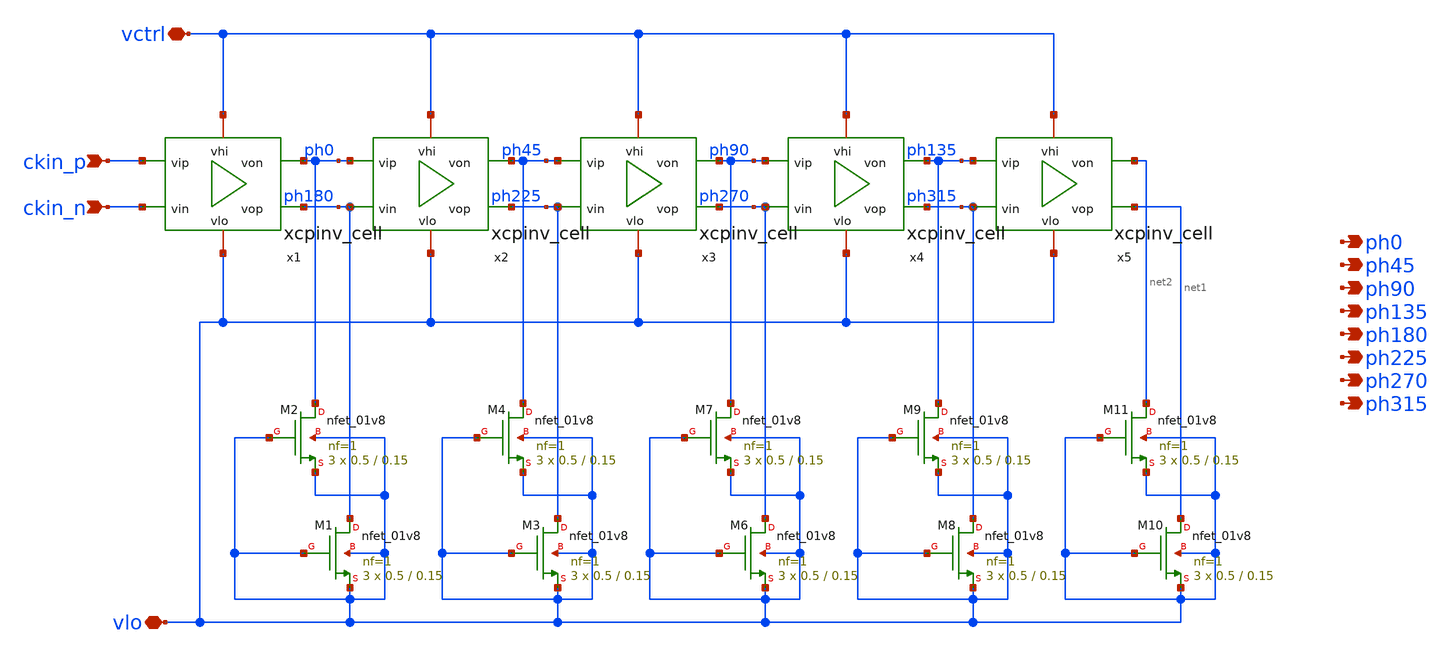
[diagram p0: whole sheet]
** sch_path: xschem/ILMPCG_delayline.sch
**.subckt ILMPCG_delayline vctrl ckin_p ckin_n ph0 ph45 ph90 ph135 ph180 ph225 ph270 ph315 vlo
*.iopin vctrl
*.ipin ckin_p
*.ipin ckin_n
*.opin ph0
*.opin ph45
*.opin ph90
*.opin ph135
*.opin ph180
*.opin ph225
*.opin ph270
*.opin ph315
*.iopin vlo
x1 vctrl ckin_p ckin_n vlo ph180 ph0 xcpinv_cell
x2 vctrl ph0 ph180 vlo ph225 ph45 xcpinv_cell
XM1 ph180 vlo vlo vlo sky130_fd_pr__nfet_01v8 L=0.15 W=0.5 nf=1 ad='int((nf+1)/2) * W/nf * 0.29' as='int((nf+2)/2) * W/nf * 0.29'
+ pd='2*int((nf+1)/2) * (W/nf + 0.29)' ps='2*int((nf+2)/2) * (W/nf + 0.29)' nrd='0.29 / W' nrs='0.29 / W'
+ sa=0 sb=0 sd=0 mult=3 m=3
XM2 ph0 vlo vlo vlo sky130_fd_pr__nfet_01v8 L=0.15 W=0.5 nf=1 ad='int((nf+1)/2) * W/nf * 0.29' as='int((nf+2)/2) * W/nf * 0.29'
+ pd='2*int((nf+1)/2) * (W/nf + 0.29)' ps='2*int((nf+2)/2) * (W/nf + 0.29)' nrd='0.29 / W' nrs='0.29 / W'
+ sa=0 sb=0 sd=0 mult=3 m=3
XM3 ph225 vlo vlo vlo sky130_fd_pr__nfet_01v8 L=0.15 W=0.5 nf=1 ad='int((nf+1)/2) * W/nf * 0.29' as='int((nf+2)/2) * W/nf * 0.29'
+ pd='2*int((nf+1)/2) * (W/nf + 0.29)' ps='2*int((nf+2)/2) * (W/nf + 0.29)' nrd='0.29 / W' nrs='0.29 / W'
+ sa=0 sb=0 sd=0 mult=3 m=3
XM4 ph45 vlo vlo vlo sky130_fd_pr__nfet_01v8 L=0.15 W=0.5 nf=1 ad='int((nf+1)/2) * W/nf * 0.29' as='int((nf+2)/2) * W/nf * 0.29'
+ pd='2*int((nf+1)/2) * (W/nf + 0.29)' ps='2*int((nf+2)/2) * (W/nf + 0.29)' nrd='0.29 / W' nrs='0.29 / W'
+ sa=0 sb=0 sd=0 mult=3 m=3
x3 vctrl ph45 ph225 vlo ph270 ph90 xcpinv_cell
XM6 ph270 vlo vlo vlo sky130_fd_pr__nfet_01v8 L=0.15 W=0.5 nf=1 ad='int((nf+1)/2) * W/nf * 0.29' as='int((nf+2)/2) * W/nf * 0.29'
+ pd='2*int((nf+1)/2) * (W/nf + 0.29)' ps='2*int((nf+2)/2) * (W/nf + 0.29)' nrd='0.29 / W' nrs='0.29 / W'
+ sa=0 sb=0 sd=0 mult=3 m=3
XM7 ph90 vlo vlo vlo sky130_fd_pr__nfet_01v8 L=0.15 W=0.5 nf=1 ad='int((nf+1)/2) * W/nf * 0.29' as='int((nf+2)/2) * W/nf * 0.29'
+ pd='2*int((nf+1)/2) * (W/nf + 0.29)' ps='2*int((nf+2)/2) * (W/nf + 0.29)' nrd='0.29 / W' nrs='0.29 / W'
+ sa=0 sb=0 sd=0 mult=3 m=3
x4 vctrl ph90 ph270 vlo ph315 ph135 xcpinv_cell
XM8 ph315 vlo vlo vlo sky130_fd_pr__nfet_01v8 L=0.15 W=0.5 nf=1 ad='int((nf+1)/2) * W/nf * 0.29' as='int((nf+2)/2) * W/nf * 0.29'
+ pd='2*int((nf+1)/2) * (W/nf + 0.29)' ps='2*int((nf+2)/2) * (W/nf + 0.29)' nrd='0.29 / W' nrs='0.29 / W'
+ sa=0 sb=0 sd=0 mult=3 m=3
XM9 ph135 vlo vlo vlo sky130_fd_pr__nfet_01v8 L=0.15 W=0.5 nf=1 ad='int((nf+1)/2) * W/nf * 0.29' as='int((nf+2)/2) * W/nf * 0.29'
+ pd='2*int((nf+1)/2) * (W/nf + 0.29)' ps='2*int((nf+2)/2) * (W/nf + 0.29)' nrd='0.29 / W' nrs='0.29 / W'
+ sa=0 sb=0 sd=0 mult=3 m=3
x5 vctrl ph135 ph315 vlo net1 net2 xcpinv_cell
XM10 net1 vlo vlo vlo sky130_fd_pr__nfet_01v8 L=0.15 W=0.5 nf=1 ad='int((nf+1)/2) * W/nf * 0.29' as='int((nf+2)/2) * W/nf * 0.29'
+ pd='2*int((nf+1)/2) * (W/nf + 0.29)' ps='2*int((nf+2)/2) * (W/nf + 0.29)' nrd='0.29 / W' nrs='0.29 / W'
+ sa=0 sb=0 sd=0 mult=3 m=3
XM11 net2 vlo vlo vlo sky130_fd_pr__nfet_01v8 L=0.15 W=0.5 nf=1 ad='int((nf+1)/2) * W/nf * 0.29' as='int((nf+2)/2) * W/nf * 0.29'
+ pd='2*int((nf+1)/2) * (W/nf + 0.29)' ps='2*int((nf+2)/2) * (W/nf + 0.29)' nrd='0.29 / W' nrs='0.29 / W'
+ sa=0 sb=0 sd=0 mult=3 m=3
**.ends

* expanding   symbol:  xcpinv_cell.sym # of pins=6
** sym_path: xschem/xcpinv_cell.sym
** sch_path: xschem/xcpinv_cell.sch
.subckt xcpinv_cell vhi vip vin vlo vop von
*.iopin vhi
*.iopin vlo
*.ipin vip
*.ipin vin
*.opin von
*.opin vop
XM1 von vip vhi vhi sky130_fd_pr__pfet_01v8 L=0.15 W=16 nf=1 ad='int((nf+1)/2) * W/nf * 0.29' as='int((nf+2)/2) * W/nf * 0.29'
+ pd='2*int((nf+1)/2) * (W/nf + 0.29)' ps='2*int((nf+2)/2) * (W/nf + 0.29)' nrd='0.29 / W' nrs='0.29 / W'
+ sa=0 sb=0 sd=0 mult=1 m=1
XM2 von vip vlo vlo sky130_fd_pr__nfet_01v8 L=0.15 W=8 nf=1 ad='int((nf+1)/2) * W/nf * 0.29' as='int((nf+2)/2) * W/nf * 0.29'
+ pd='2*int((nf+1)/2) * (W/nf + 0.29)' ps='2*int((nf+2)/2) * (W/nf + 0.29)' nrd='0.29 / W' nrs='0.29 / W'
+ sa=0 sb=0 sd=0 mult=1 m=1
XM3 von vop vhi vhi sky130_fd_pr__pfet_01v8 L=0.15 W=8 nf=1 ad='int((nf+1)/2) * W/nf * 0.29' as='int((nf+2)/2) * W/nf * 0.29'
+ pd='2*int((nf+1)/2) * (W/nf + 0.29)' ps='2*int((nf+2)/2) * (W/nf + 0.29)' nrd='0.29 / W' nrs='0.29 / W'
+ sa=0 sb=0 sd=0 mult=1 m=1
XM4 von vop vlo vlo sky130_fd_pr__nfet_01v8 L=0.15 W=4 nf=1 ad='int((nf+1)/2) * W/nf * 0.29' as='int((nf+2)/2) * W/nf * 0.29'
+ pd='2*int((nf+1)/2) * (W/nf + 0.29)' ps='2*int((nf+2)/2) * (W/nf + 0.29)' nrd='0.29 / W' nrs='0.29 / W'
+ sa=0 sb=0 sd=0 mult=1 m=1
XM5 vop von vhi vhi sky130_fd_pr__pfet_01v8 L=0.15 W=8 nf=1 ad='int((nf+1)/2) * W/nf * 0.29' as='int((nf+2)/2) * W/nf * 0.29'
+ pd='2*int((nf+1)/2) * (W/nf + 0.29)' ps='2*int((nf+2)/2) * (W/nf + 0.29)' nrd='0.29 / W' nrs='0.29 / W'
+ sa=0 sb=0 sd=0 mult=1 m=1
XM6 vop von vlo vlo sky130_fd_pr__nfet_01v8 L=0.15 W=4 nf=1 ad='int((nf+1)/2) * W/nf * 0.29' as='int((nf+2)/2) * W/nf * 0.29'
+ pd='2*int((nf+1)/2) * (W/nf + 0.29)' ps='2*int((nf+2)/2) * (W/nf + 0.29)' nrd='0.29 / W' nrs='0.29 / W'
+ sa=0 sb=0 sd=0 mult=1 m=1
XM7 vop vin vhi vhi sky130_fd_pr__pfet_01v8 L=0.15 W=16 nf=1 ad='int((nf+1)/2) * W/nf * 0.29' as='int((nf+2)/2) * W/nf * 0.29'
+ pd='2*int((nf+1)/2) * (W/nf + 0.29)' ps='2*int((nf+2)/2) * (W/nf + 0.29)' nrd='0.29 / W' nrs='0.29 / W'
+ sa=0 sb=0 sd=0 mult=1 m=1
XM8 vop vin vlo vlo sky130_fd_pr__nfet_01v8 L=0.15 W=8 nf=1 ad='int((nf+1)/2) * W/nf * 0.29' as='int((nf+2)/2) * W/nf * 0.29'
+ pd='2*int((nf+1)/2) * (W/nf + 0.29)' ps='2*int((nf+2)/2) * (W/nf + 0.29)' nrd='0.29 / W' nrs='0.29 / W'
+ sa=0 sb=0 sd=0 mult=1 m=1
.ends

.end
